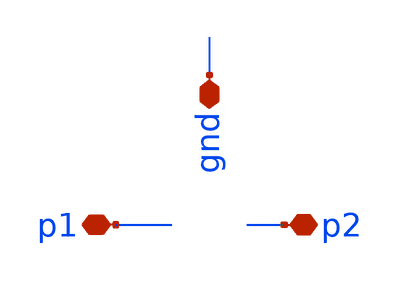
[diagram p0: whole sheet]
** sch_path: MICRO/lc_filter_pex_xschem.sch
**.subckt lc_filter_pex_xschem p1 p2 gnd
*.iopin p1
*.iopin p2
*.iopin gnd
**** begin user architecture code


* SPICE3 file created from lc_filter_pex_magic.ext - technology: sky130A

*.option scale=5000u

.subckt lc_filter_pex_xschem p1 p2 gnd
X0 p1 p2 sky130_fd_pr__cap_mim_m3_2 l=22.3 w=22.3
X1 p1 p2 sky130_fd_pr__cap_mim_m3_2 l=22.3 w=22.3
X2 p1 p2 sky130_fd_pr__cap_mim_m3_2 l=22.3 w=22.3
X3 p1 p2 sky130_fd_pr__cap_mim_m3_2 l=22.3 w=22.3
C0 p1 p2 167.71fF
C1 p1 gnd 0.49fF
C2 p2 gnd 33.62fF
.ends
.end


**** end user architecture code
**.ends
.end
